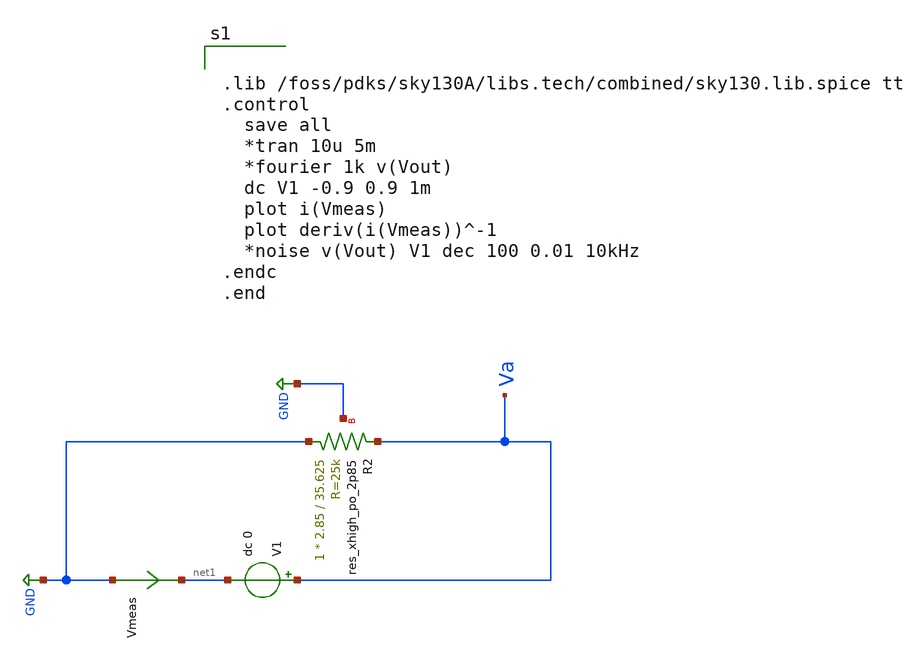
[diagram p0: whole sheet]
** sch_path: xschem/Res_TB.sch
**.subckt Res_TB
V1 Va net1 dc 0
Vmeas GND net1 0
.save i(vmeas)
XR2 GND Va GND sky130_fd_pr__res_xhigh_po_2p85 L=35.625 mult=1 m=1
**** begin user architecture code


.lib /foss/pdks/sky130A/libs.tech/combined/sky130.lib.spice tt
.control
  save all
  *tran 10u 5m
  *fourier 1k v(Vout)
  dc V1 -0.9 0.9 1m
  plot i(Vmeas)
  plot deriv(i(Vmeas))^-1
  *noise v(Vout) V1 dec 100 0.01 10kHz
.endc
.end

**** end user architecture code
**.ends
.GLOBAL GND
.end
